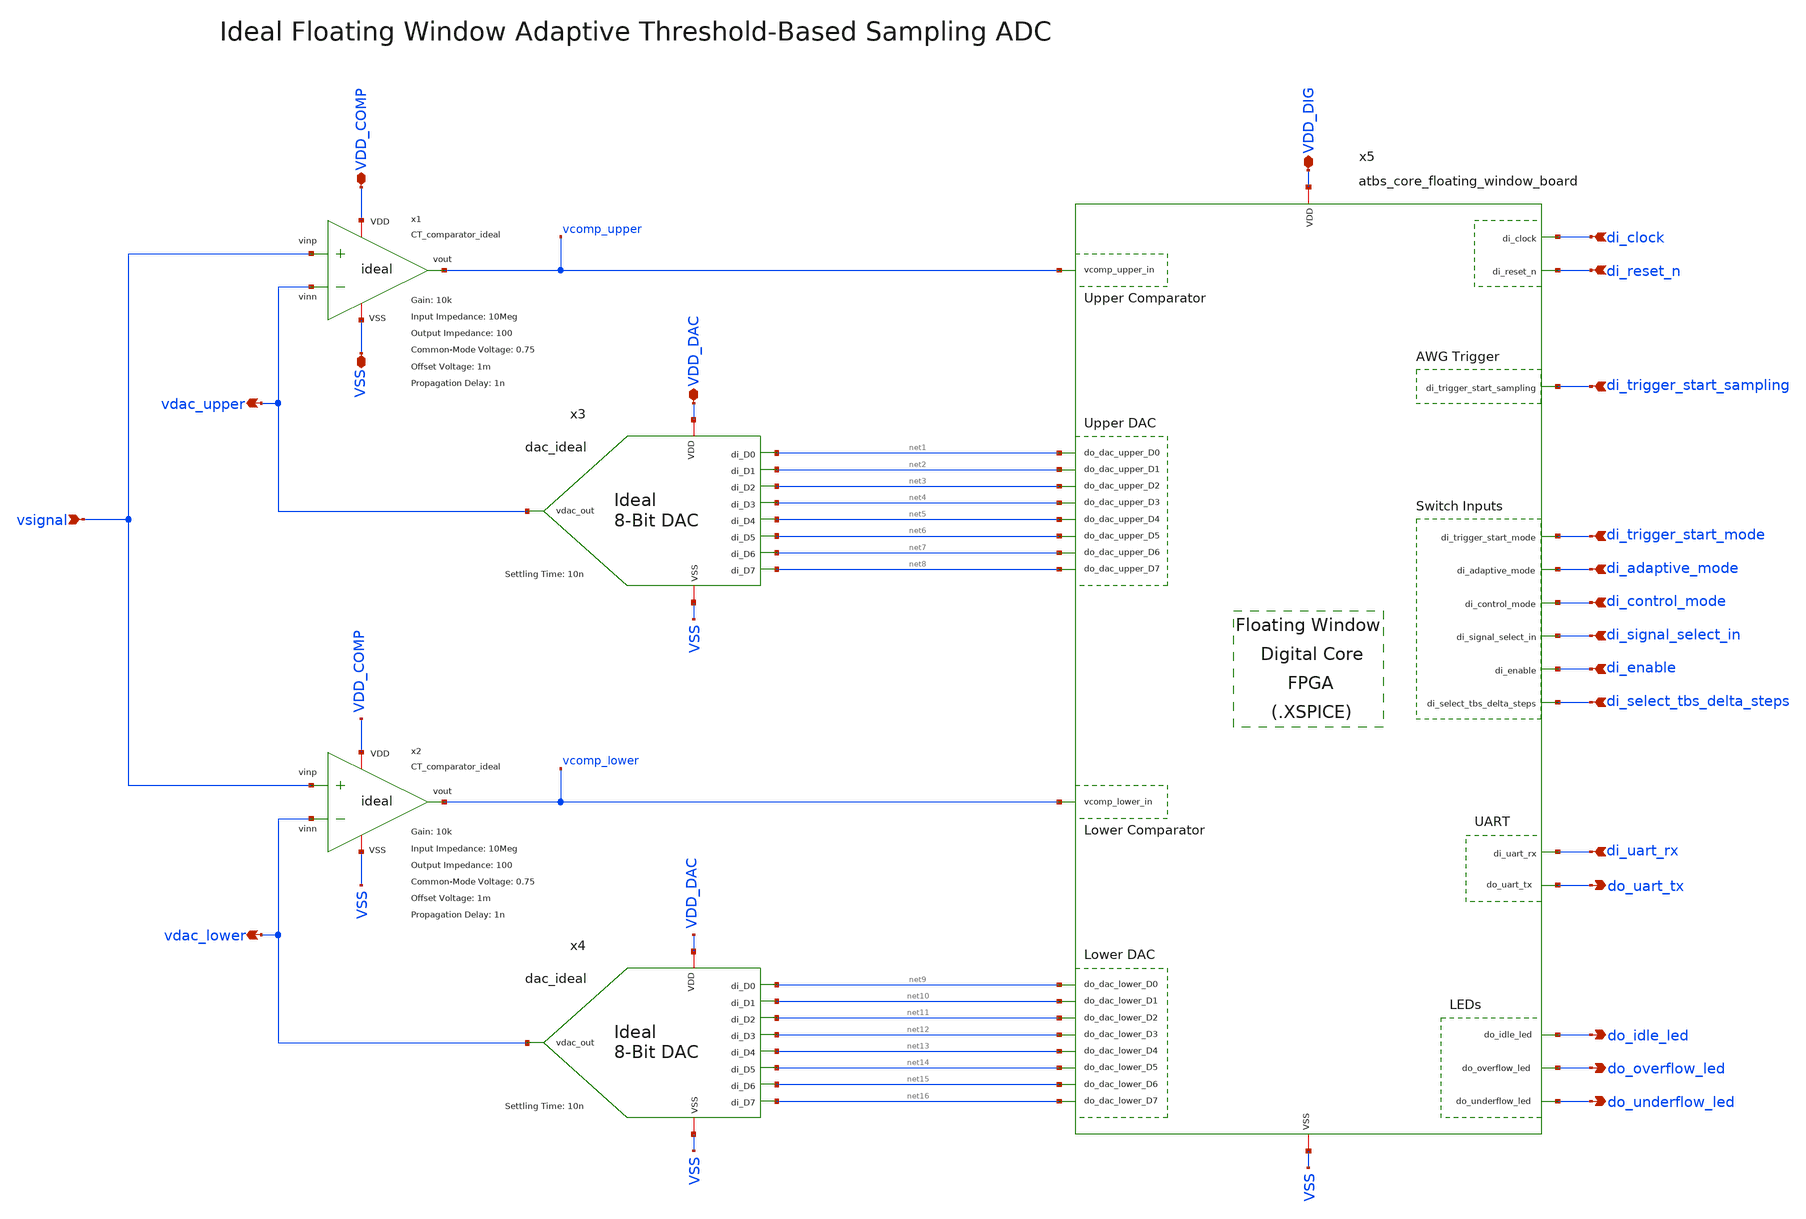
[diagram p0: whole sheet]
** sch_path: SG13G2_ATBS-ADC-main/xschem/top_level/atbs_top_floating_window_ideal.sch
**.subckt atbs_top_floating_window_ideal VDD_DIG VSS VDD_COMP vsignal di_clock di_reset_n VDD_DAC
*+ di_uart_rx do_uart_tx di_trigger_start_sampling di_trigger_start_mode di_adaptive_mode di_control_mode
*+ di_signal_select_in di_enable di_select_tbs_delta_steps do_idle_led do_overflow_led do_underflow_led vdac_upper
*+ vdac_lower
*.iopin VDD_DIG
*.iopin VSS
*.iopin VDD_COMP
*.ipin vsignal
*.ipin di_clock
*.ipin di_reset_n
*.iopin VDD_DAC
*.ipin di_uart_rx
*.opin do_uart_tx
*.ipin di_trigger_start_sampling
*.ipin di_trigger_start_mode
*.ipin di_adaptive_mode
*.ipin di_control_mode
*.ipin di_signal_select_in
*.ipin di_enable
*.ipin di_select_tbs_delta_steps
*.opin do_idle_led
*.opin do_overflow_led
*.opin do_underflow_led
*.opin vdac_upper
*.opin vdac_lower
x5 VDD_DIG VSS di_adaptive_mode di_clock vcomp_lower vcomp_upper di_control_mode net9 net10 net11
+ net12 net13 net14 net15 net16 net1 net2 net3 net4 net5 net6 net7 net8 di_enable do_idle_led
+ do_overflow_led di_reset_n di_select_tbs_delta_steps di_signal_select_in di_trigger_start_mode
+ di_trigger_start_sampling di_uart_rx do_uart_tx do_underflow_led atbs_core_floating_window_board
x3 VDD_DAC net2 net5 net1 net3 net4 net8 net6 net7 vdac_upper VSS dac_ideal tsettle=10n
x4 VDD_DAC net10 net13 net9 net11 net12 net16 net14 net15 vdac_lower VSS dac_ideal tsettle=10n
x1 vsignal vdac_upper VDD_COMP vcomp_upper VSS CT_comparator_ideal A=10k Rin=10Meg Rout=100 Pdc=
+ Vcm=0.75 Voffs=1m tpd=1n
x2 vsignal vdac_lower VDD_COMP vcomp_lower VSS CT_comparator_ideal A=10k Rin=10Meg Rout=100 Pdc=
+ Vcm=0.75 Voffs=1m tpd=1n
**.ends

* expanding   symbol:  dac/ideal/dac_ideal.sym # of pins=11
** sym_path: SG13G2_ATBS-ADC-main/xschem/dac/ideal/dac_ideal.sym
** sch_path: SG13G2_ATBS-ADC-main/xschem/dac/ideal/dac_ideal.sch
.subckt dac_ideal VDD di_D1 di_D4 di_D0 di_D2 di_D3 di_D7 di_D5 di_D6 vdac_out VSS  tsettle=10n
*.opin vdac_out
*.ipin di_D0
*.iopin VSS
*.iopin VDD
*.ipin di_D1
*.ipin di_D2
*.ipin di_D3
*.ipin di_D4
*.ipin di_D5
*.ipin di_D6
*.ipin di_D7
R1 net1 VSS 3925 m=1
G1 VDD net1 di_D0 VSS 1u
G2 VDD net1 di_D1 VSS 2u
G3 VDD net1 di_D2 VSS 4u
G4 VDD net1 di_D3 VSS 8u
G5 VDD net1 di_D4 VSS 16u
G6 VDD net1 di_D5 VSS 32u
G7 VDD net1 di_D6 VSS 64u
G8 VDD net1 di_D7 VSS 128u
A1 net1 vdac_out VSS del_subckt
.model del_subckt delay(delay=tsettle buffer_size=8192)
.ends


* expanding   symbol:  comparator/continuous_time/ideal/CT_comparator_ideal.sym # of pins=5
** sym_path: SG13G2_ATBS-ADC-main/xschem/comparator/continuous_time/ideal/CT_comparator_ideal.sym
** sch_path: SG13G2_ATBS-ADC-main/xschem/comparator/continuous_time/ideal/CT_comparator_ideal.sch
.subckt CT_comparator_ideal vinp vinn VDD vout VSS  A=10k Rin=10Meg Rout=100 Vcm=0.75 Voffs=1m
+ tpd=1n
*.ipin vinn
*.opin vout
*.ipin vinp
*.iopin VSS
*.iopin VDD
R1 vinp vinn {Rin} m=1
B1 net1 VSS v=v(VDD)/2*tanh({A}/(v(VDD)/2)*(v(vinp)-v(vinn)-{Voffs}))+{Vcm}
R3 net2 vout {Rout} m=1
A1 net1 net2 VSS del_subckt
.model del_subckt delay(delay=tpd buffer_size=8192)
.ends

.end
